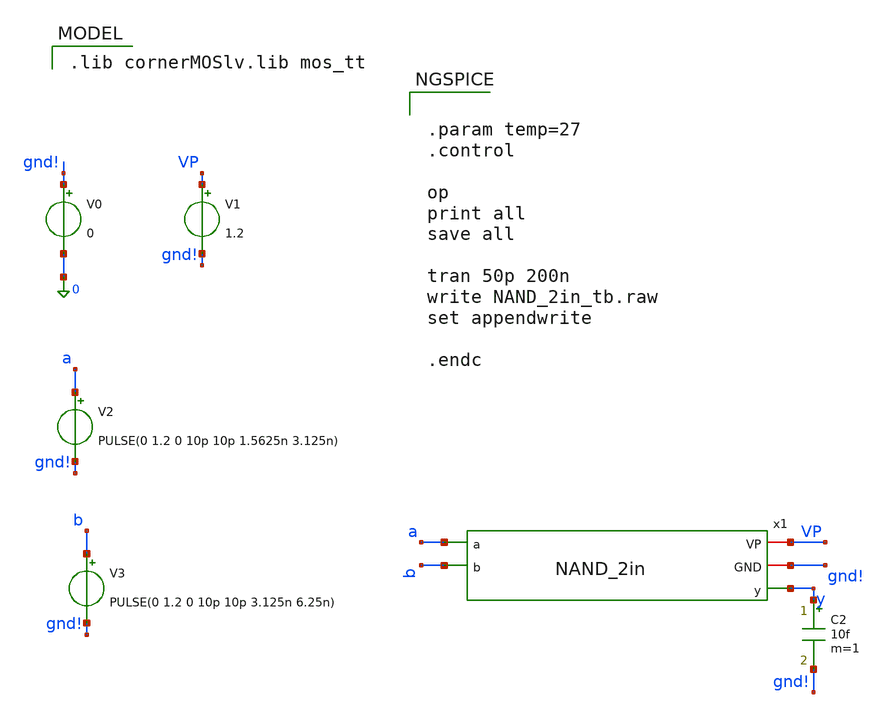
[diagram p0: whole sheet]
** sch_path: schematics/divider/tb/NAND_2in_tb.sch
**.subckt NAND_2in_tb
V1 VP gnd! 1.2
V2 a gnd! PULSE(0 1.2 0 10p 10p 1.5625n 3.125n)
V0 gnd! 0 0
C2 y gnd! 10f m=1
V3 b gnd! PULSE(0 1.2 0 10p 10p 3.125n 6.25n)
x1 VP gnd! a y b NAND_2in
**** begin user architecture code
 .lib cornerMOSlv.lib mos_tt



.param temp=27
.control

op
print all
save all

tran 50p 200n
write NAND_2in_tb.raw
set appendwrite

.endc


**** end user architecture code
**.ends

* expanding   symbol:  /foss/designs/CHIP-PLL/divider/schematics/NAND_2in.sym # of pins=5
** sym_path: schematics/divider/schematics/NAND_2in.sym
** sch_path: schematics/divider/schematics/NAND_2in.sch
.subckt NAND_2in VP GND a y b
*.opin y
*.iopin GND
*.ipin a
*.iopin VP
*.ipin b
XM1 y a net1 GND sg13_lv_nmos w=0.15u l=0.13u ng=1 m=1 mm_ok=1
XM3 net1 b GND GND sg13_lv_nmos w=0.15u l=0.13u ng=1 m=1 mm_ok=1
XM2 y b VP VP sg13_lv_pmos w=0.15u l=0.13u ng=1 m=1 mm_ok=1
XM4 y a VP VP sg13_lv_pmos w=0.15u l=0.13u ng=1 m=1 mm_ok=1
.ends

.end
